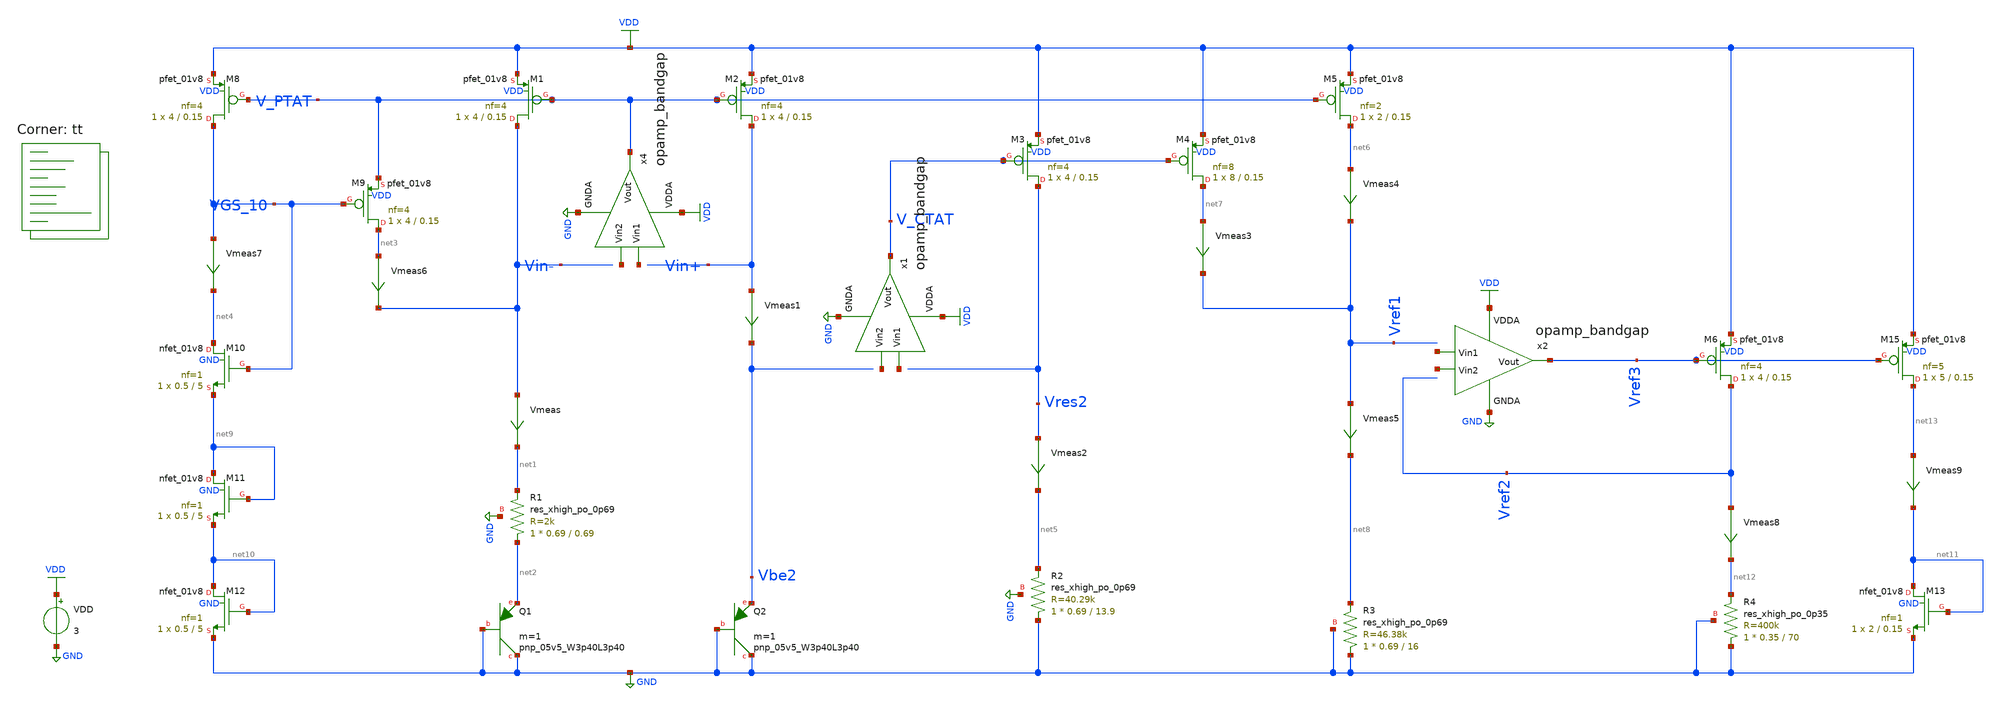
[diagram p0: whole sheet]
** sch_path: projects/bandgapref/xschem_ngspice/new_files/tb_low_voltage_BGR.sch
**.subckt tb_low_voltage_BGR
VDD VDD GND 3
Vmeas Vin- net1 0
.save i(vmeas)
Vmeas1 Vin+ Vbe2 0
.save i(vmeas1)
XR1 net2 net1 GND sky130_fd_pr__res_xhigh_po_0p69 L=0.69 mult=1 m=1
XM1 Vin- V_PTAT VDD VDD sky130_fd_pr__pfet_01v8 L=0.15 W=4 nf=4 ad='int((nf+1)/2) * W/nf * 0.29' as='int((nf+2)/2) * W/nf * 0.29'
+ pd='2*int((nf+1)/2) * (W/nf + 0.29)' ps='2*int((nf+2)/2) * (W/nf + 0.29)' nrd='0.29 / W' nrs='0.29 / W'
+ sa=0 sb=0 sd=0 mult=1 m=1
XM2 Vin+ V_PTAT VDD VDD sky130_fd_pr__pfet_01v8 L=0.15 W=4 nf=4 ad='int((nf+1)/2) * W/nf * 0.29' as='int((nf+2)/2) * W/nf * 0.29'
+ pd='2*int((nf+1)/2) * (W/nf + 0.29)' ps='2*int((nf+2)/2) * (W/nf + 0.29)' nrd='0.29 / W' nrs='0.29 / W'
+ sa=0 sb=0 sd=0 mult=1 m=1
XR2 GND net5 GND sky130_fd_pr__res_xhigh_po_0p69 L=13.9 mult=1 m=1
XM3 Vres2 V_CTAT VDD VDD sky130_fd_pr__pfet_01v8 L=0.15 W=4 nf=4 ad='int((nf+1)/2) * W/nf * 0.29' as='int((nf+2)/2) * W/nf * 0.29'
+ pd='2*int((nf+1)/2) * (W/nf + 0.29)' ps='2*int((nf+2)/2) * (W/nf + 0.29)' nrd='0.29 / W' nrs='0.29 / W'
+ sa=0 sb=0 sd=0 mult=1 m=1
XM4 net7 V_CTAT VDD VDD sky130_fd_pr__pfet_01v8 L=0.15 W=8 nf=8 ad='int((nf+1)/2) * W/nf * 0.29' as='int((nf+2)/2) * W/nf * 0.29'
+ pd='2*int((nf+1)/2) * (W/nf + 0.29)' ps='2*int((nf+2)/2) * (W/nf + 0.29)' nrd='0.29 / W' nrs='0.29 / W'
+ sa=0 sb=0 sd=0 mult=1 m=1
XM5 net6 V_PTAT VDD VDD sky130_fd_pr__pfet_01v8 L=0.15 W=2 nf=2 ad='int((nf+1)/2) * W/nf * 0.29' as='int((nf+2)/2) * W/nf * 0.29'
+ pd='2*int((nf+1)/2) * (W/nf + 0.29)' ps='2*int((nf+2)/2) * (W/nf + 0.29)' nrd='0.29 / W' nrs='0.29 / W'
+ sa=0 sb=0 sd=0 mult=1 m=1
XR3 GND net8 GND sky130_fd_pr__res_xhigh_po_0p69 L=16 mult=1 m=1
XM8 VGS_10 V_PTAT VDD VDD sky130_fd_pr__pfet_01v8 L=0.15 W=4 nf=4 ad='int((nf+1)/2) * W/nf * 0.29' as='int((nf+2)/2) * W/nf * 0.29'
+ pd='2*int((nf+1)/2) * (W/nf + 0.29)' ps='2*int((nf+2)/2) * (W/nf + 0.29)' nrd='0.29 / W' nrs='0.29 / W'
+ sa=0 sb=0 sd=0 mult=1 m=1
XM9 net3 VGS_10 V_PTAT VDD sky130_fd_pr__pfet_01v8 L=0.15 W=4 nf=4 ad='int((nf+1)/2) * W/nf * 0.29' as='int((nf+2)/2) * W/nf * 0.29'
+ pd='2*int((nf+1)/2) * (W/nf + 0.29)' ps='2*int((nf+2)/2) * (W/nf + 0.29)' nrd='0.29 / W' nrs='0.29 / W'
+ sa=0 sb=0 sd=0 mult=1 m=1
XM10 net4 VGS_10 net9 GND sky130_fd_pr__nfet_01v8 L=5 W=0.5 nf=1 ad='int((nf+1)/2) * W/nf * 0.29' as='int((nf+2)/2) * W/nf * 0.29'
+ pd='2*int((nf+1)/2) * (W/nf + 0.29)' ps='2*int((nf+2)/2) * (W/nf + 0.29)' nrd='0.29 / W' nrs='0.29 / W'
+ sa=0 sb=0 sd=0 mult=1 m=1
Vmeas2 Vres2 net5 0
.save i(vmeas2)
Vmeas3 net7 Vref1 0
.save i(vmeas3)
Vmeas4 net6 Vref1 0
.save i(vmeas4)
Vmeas5 Vref1 net8 0
.save i(vmeas5)
Vmeas6 net3 Vin- 0
.save i(vmeas6)
Vmeas7 VGS_10 net4 0
.save i(vmeas7)
XM11 net9 net9 net10 GND sky130_fd_pr__nfet_01v8 L=5 W=0.5 nf=1 ad='int((nf+1)/2) * W/nf * 0.29' as='int((nf+2)/2) * W/nf * 0.29'
+ pd='2*int((nf+1)/2) * (W/nf + 0.29)' ps='2*int((nf+2)/2) * (W/nf + 0.29)' nrd='0.29 / W' nrs='0.29 / W'
+ sa=0 sb=0 sd=0 mult=1 m=1
XM12 net10 net10 GND GND sky130_fd_pr__nfet_01v8 L=5 W=0.5 nf=1 ad='int((nf+1)/2) * W/nf * 0.29' as='int((nf+2)/2) * W/nf * 0.29'
+ pd='2*int((nf+1)/2) * (W/nf + 0.29)' ps='2*int((nf+2)/2) * (W/nf + 0.29)' nrd='0.29 / W' nrs='0.29 / W'
+ sa=0 sb=0 sd=0 mult=1 m=1
XM6 Vref2 Vref3 VDD VDD sky130_fd_pr__pfet_01v8 L=0.15 W=4 nf=4 ad='int((nf+1)/2) * W/nf * 0.29' as='int((nf+2)/2) * W/nf * 0.29'
+ pd='2*int((nf+1)/2) * (W/nf + 0.29)' ps='2*int((nf+2)/2) * (W/nf + 0.29)' nrd='0.29 / W' nrs='0.29 / W'
+ sa=0 sb=0 sd=0 mult=1 m=1
XM13 net11 net11 GND GND sky130_fd_pr__nfet_01v8 L=0.15 W=2 nf=1 ad='int((nf+1)/2) * W/nf * 0.29' as='int((nf+2)/2) * W/nf * 0.29'
+ pd='2*int((nf+1)/2) * (W/nf + 0.29)' ps='2*int((nf+2)/2) * (W/nf + 0.29)' nrd='0.29 / W' nrs='0.29 / W'
+ sa=0 sb=0 sd=0 mult=1 m=1
Vmeas8 Vref2 net12 0
.save i(vmeas8)
Vmeas9 net13 net11 0
.save i(vmeas9)
XM15 net13 Vref3 VDD VDD sky130_fd_pr__pfet_01v8 L=0.15 W=5 nf=5 ad='int((nf+1)/2) * W/nf * 0.29' as='int((nf+2)/2) * W/nf * 0.29'
+ pd='2*int((nf+1)/2) * (W/nf + 0.29)' ps='2*int((nf+2)/2) * (W/nf + 0.29)' nrd='0.29 / W' nrs='0.29 / W'
+ sa=0 sb=0 sd=0 mult=1 m=1
XR4 GND net12 GND sky130_fd_pr__res_xhigh_po_0p35 L=70 mult=1 m=1
x4 VDD V_PTAT net14 net15 GND opamp_bandgap
x1 VDD V_CTAT net16 net17 GND opamp_bandgap
x2 VDD Vref3 net18 net19 GND opamp_bandgap
XQ1 GND GND net2 sky130_fd_pr__pnp_05v5_W3p40L3p40 m=1
XQ2 GND GND Vbe2 sky130_fd_pr__pnp_05v5_W3p40L3p40 m=1
**** begin user architecture code
.lib $::SKYWATER_MODELS/sky130.lib.spice tt



.option method=gear
.option wnflag=1
.option savecurrents

.save @m.xm1.msky130_fd_pr__pfet_01v8[gm] @m.xm2.msky130_fd_pr__pfet_01v8[gm] @m.xm3.msky130_fd_pr__pfet_01v8[gm] @m.xm4.msky130_fd_pr__pfet_01v8[gm] @m.xm5.msky130_fd_pr__pfet_01v8[gm] @m.xm6.msky130_fd_pr__pfet_01v8[gm] @m.xm7.msky130_fd_pr__pfet_01v8[gm] @m.xm8.msky130_fd_pr__pfet_01v8[gm] @m.xm9.msky130_fd_pr__pfet_01v8[gm] @m.xm10.msky130_fd_pr__nfet_01v8[gm] @m.xm11.msky130_fd_pr__nfet_01v8[gm] @m.xm12.msky130_fd_pr__nfet_01v8[gm]


.control
  save all
  op
  dc temp -40 120 1 VDD 1.6 3.3 0.1
  * tran 1ns 40us
  remzerovec
  write tb_low_voltage_BGR.raw
  set appendwrite
.endc




**** end user architecture code
**.ends

* expanding   symbol:  opamp_bandgap.sym # of pins=5
** sym_path: projects/pll/bandgapref/xschem_ngspice/opamp_bandgap.sym
** sch_path: projects/pll/bandgapref/xschem_ngspice/opamp_bandgap.sch
.subckt opamp_bandgap VDDA Vout Vin2 Vin1 GNDA
*.ipin Vin1
*.opin Vout
*.ipin Vin2
*.ipin GNDA
*.ipin VDDA
XM2 net1 Vin1 net2 GNDA sky130_fd_pr__nfet_01v8 L=0.15 W=1 nf=1 ad='int((nf+1)/2) * W/nf * 0.29' as='int((nf+2)/2) * W/nf * 0.29'
+ pd='2*int((nf+1)/2) * (W/nf + 0.29)' ps='2*int((nf+2)/2) * (W/nf + 0.29)' nrd='0.29 / W' nrs='0.29 / W'
+ sa=0 sb=0 sd=0 mult=1 m=1
XM3 Vout Vin2 net2 GNDA sky130_fd_pr__nfet_01v8 L=0.15 W=1 nf=1 ad='int((nf+1)/2) * W/nf * 0.29' as='int((nf+2)/2) * W/nf * 0.29'
+ pd='2*int((nf+1)/2) * (W/nf + 0.29)' ps='2*int((nf+2)/2) * (W/nf + 0.29)' nrd='0.29 / W' nrs='0.29 / W'
+ sa=0 sb=0 sd=0 mult=1 m=1
XM4 net1 net1 VDDA VDDA sky130_fd_pr__pfet_01v8 L=0.15 W=2 nf=1 ad='int((nf+1)/2) * W/nf * 0.29' as='int((nf+2)/2) * W/nf * 0.29'
+ pd='2*int((nf+1)/2) * (W/nf + 0.29)' ps='2*int((nf+2)/2) * (W/nf + 0.29)' nrd='0.29 / W' nrs='0.29 / W'
+ sa=0 sb=0 sd=0 mult=1 m=1
XM5 Vout net1 VDDA VDDA sky130_fd_pr__pfet_01v8 L=0.15 W=2 nf=1 ad='int((nf+1)/2) * W/nf * 0.29' as='int((nf+2)/2) * W/nf * 0.29'
+ pd='2*int((nf+1)/2) * (W/nf + 0.29)' ps='2*int((nf+2)/2) * (W/nf + 0.29)' nrd='0.29 / W' nrs='0.29 / W'
+ sa=0 sb=0 sd=0 mult=1 m=1
XM1 net2 net2 GNDA GNDA sky130_fd_pr__nfet_01v8 L=0.15 W=1 nf=1 ad='int((nf+1)/2) * W/nf * 0.29' as='int((nf+2)/2) * W/nf * 0.29'
+ pd='2*int((nf+1)/2) * (W/nf + 0.29)' ps='2*int((nf+2)/2) * (W/nf + 0.29)' nrd='0.29 / W' nrs='0.29 / W'
+ sa=0 sb=0 sd=0 mult=1 m=1
.ends

.GLOBAL GND
.GLOBAL VDD
.end
